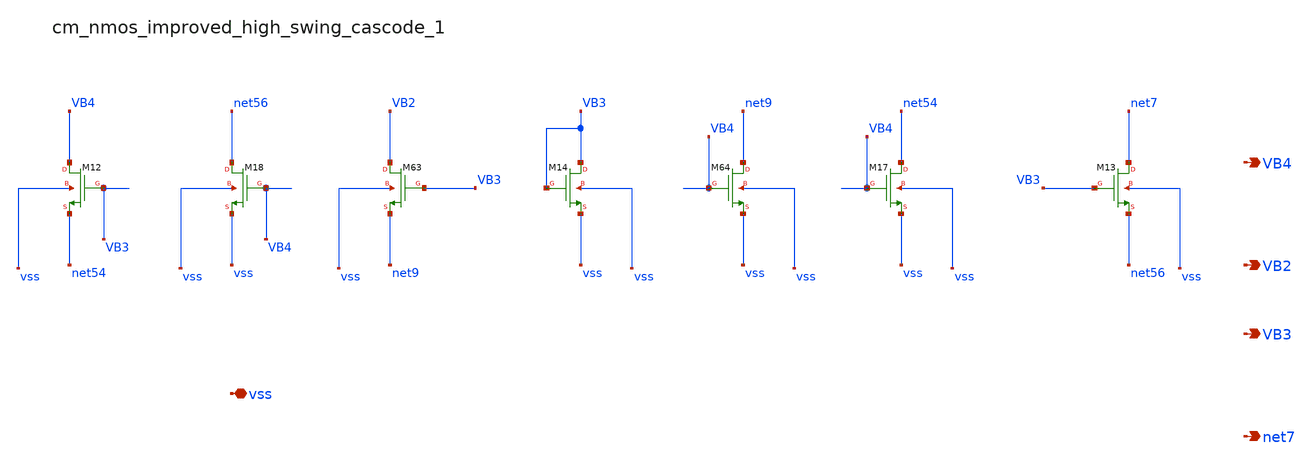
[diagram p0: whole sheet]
** sch_path: analog-db/raw/amp_012_peng_tcfc/hier/blocks/cm_nmos_improved_high_swing_cascode_1.sch
**.subckt cm_nmos_improved_high_swing_cascode_1 vss VB4 VB2 VB3 net7
*.iopin vss
*.opin VB4
*.opin VB2
*.opin VB3
*.opin net7
XM12 VB4 VB3 net54 vss sg13_lv_nmos w=x_dut_xm12_w l=x_dut_xm12_l ng=1 m=x_dut_xm12_m
XM13 net7 VB3 net56 vss sg13_lv_nmos w=x_dut_xm13_w l=x_dut_xm13_l ng=1 m=x_dut_xm13_m
XM14 VB3 VB3 vss vss sg13_lv_nmos w=x_dut_xm14_w l=x_dut_xm14_l ng=1 m=x_dut_xm14_m
XM17 net54 VB4 vss vss sg13_lv_nmos w=x_dut_xm17_w l=x_dut_xm17_l ng=1 m=x_dut_xm17_m
XM18 net56 VB4 vss vss sg13_lv_nmos w=x_dut_xm18_w l=x_dut_xm18_l ng=1 m=x_dut_xm18_m
XM63 VB2 VB3 net9 vss sg13_lv_nmos w=x_dut_xm63_w l=x_dut_xm63_l ng=1 m=x_dut_xm63_m
XM64 net9 VB4 vss vss sg13_lv_nmos w=x_dut_xm64_w l=x_dut_xm64_l ng=1 m=x_dut_xm64_m
**.ends
.end
